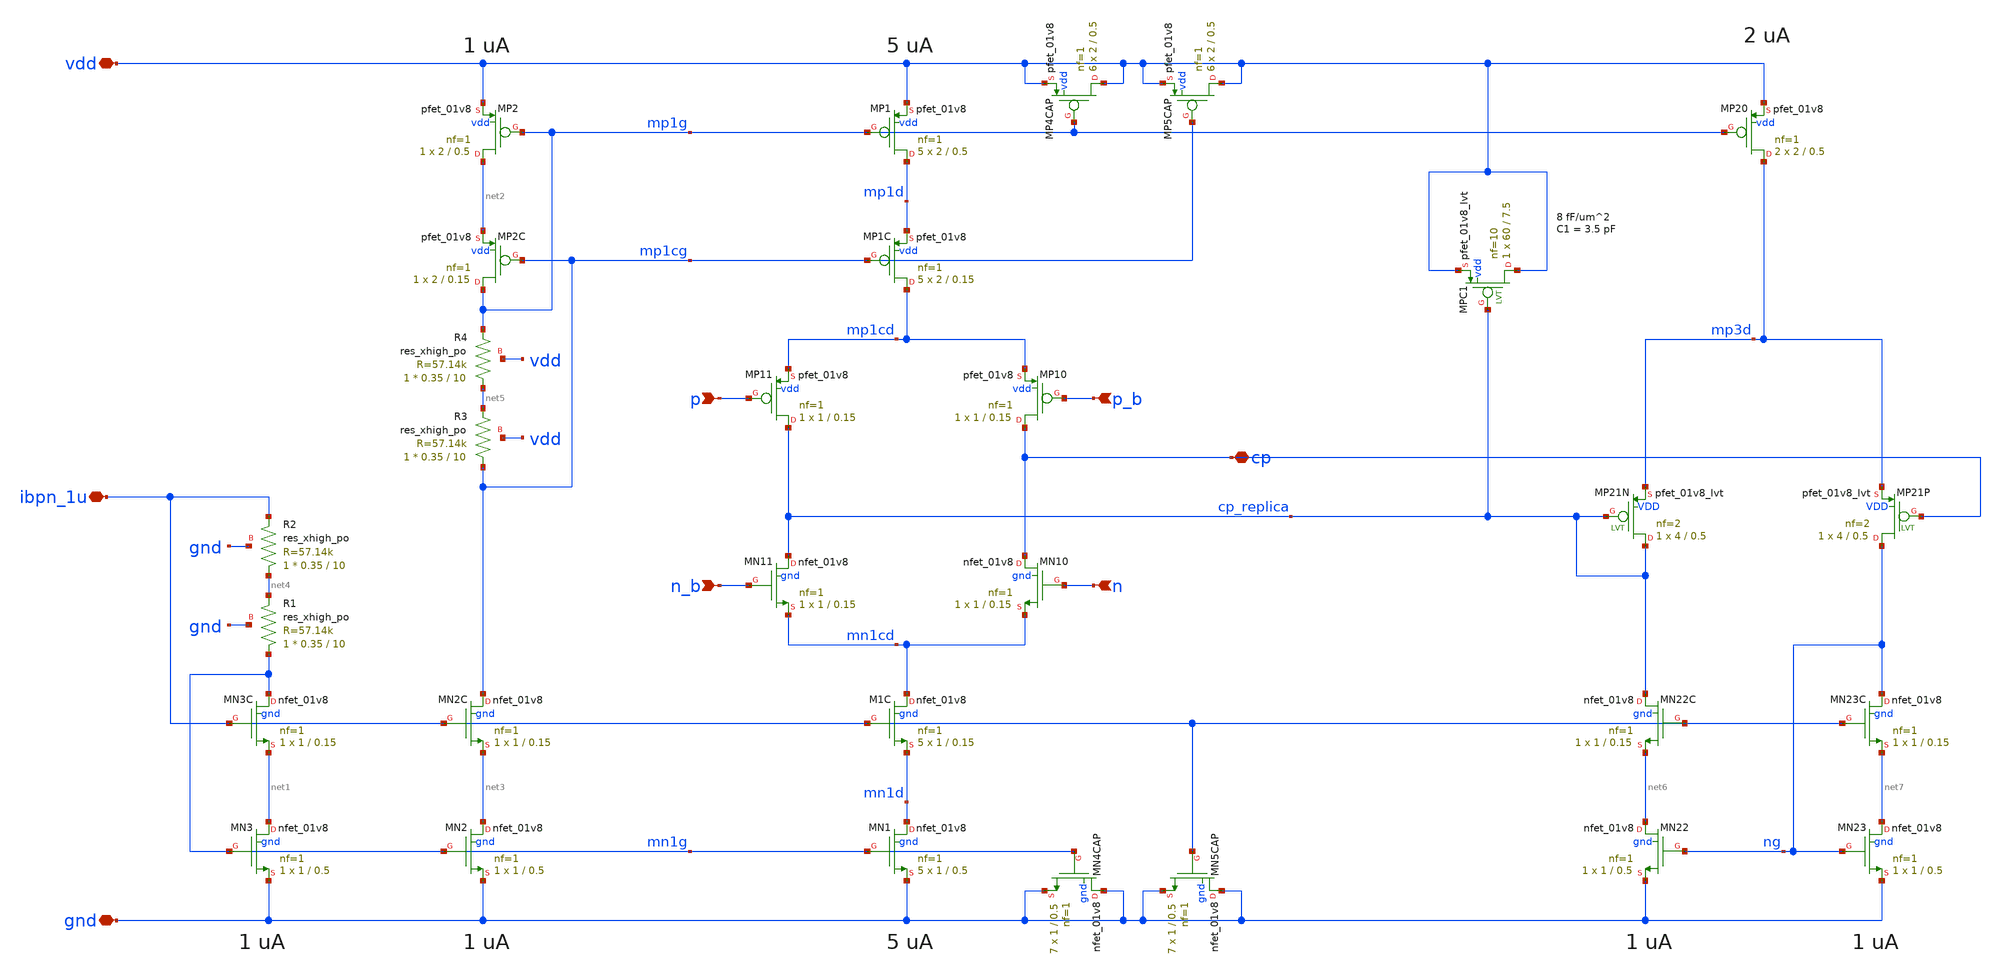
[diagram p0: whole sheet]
** sch_path: xschem/ejf_pll96_chp.sch
**.subckt ejf_pll96_chp vdd gnd ibpn_1u cp p n_b p_b n
*.iopin vdd
*.iopin gnd
*.iopin ibpn_1u
*.iopin cp
*.ipin p
*.ipin n_b
*.ipin p_b
*.ipin n
XMN3 net1 mn1g gnd gnd sky130_fd_pr__nfet_01v8 L=0.5 W=1 nf=1 ad='int((nf+1)/2) * W/nf * 0.29' as='int((nf+2)/2) * W/nf * 0.29'
+ pd='2*int((nf+1)/2) * (W/nf + 0.29)' ps='2*int((nf+2)/2) * (W/nf + 0.29)' nrd='0.29 / W' nrs='0.29 / W'
+ sa=0 sb=0 sd=0 mult=1 m=1
XMN3C mn1g ibpn_1u net1 gnd sky130_fd_pr__nfet_01v8 L=0.15 W=1 nf=1 ad='int((nf+1)/2) * W/nf * 0.29'
+ as='int((nf+2)/2) * W/nf * 0.29' pd='2*int((nf+1)/2) * (W/nf + 0.29)' ps='2*int((nf+2)/2) * (W/nf + 0.29)'
+ nrd='0.29 / W' nrs='0.29 / W' sa=0 sb=0 sd=0 mult=1 m=1
XMP2 net2 mp1g vdd vdd sky130_fd_pr__pfet_01v8 L=0.5 W=2 nf=1 ad='int((nf+1)/2) * W/nf * 0.29' as='int((nf+2)/2) * W/nf * 0.29'
+ pd='2*int((nf+1)/2) * (W/nf + 0.29)' ps='2*int((nf+2)/2) * (W/nf + 0.29)' nrd='0.29 / W' nrs='0.29 / W'
+ sa=0 sb=0 sd=0 mult=1 m=1
XMN2 net3 mn1g gnd gnd sky130_fd_pr__nfet_01v8 L=0.5 W=1 nf=1 ad='int((nf+1)/2) * W/nf * 0.29' as='int((nf+2)/2) * W/nf * 0.29'
+ pd='2*int((nf+1)/2) * (W/nf + 0.29)' ps='2*int((nf+2)/2) * (W/nf + 0.29)' nrd='0.29 / W' nrs='0.29 / W'
+ sa=0 sb=0 sd=0 mult=1 m=1
XMN2C mp1cg ibpn_1u net3 gnd sky130_fd_pr__nfet_01v8 L=0.15 W=1 nf=1 ad='int((nf+1)/2) * W/nf * 0.29'
+ as='int((nf+2)/2) * W/nf * 0.29' pd='2*int((nf+1)/2) * (W/nf + 0.29)' ps='2*int((nf+2)/2) * (W/nf + 0.29)'
+ nrd='0.29 / W' nrs='0.29 / W' sa=0 sb=0 sd=0 mult=1 m=1
XMP1 mp1d mp1g vdd vdd sky130_fd_pr__pfet_01v8 L=0.5 W=2 nf=1 ad='int((nf+1)/2) * W/nf * 0.29' as='int((nf+2)/2) * W/nf * 0.29'
+ pd='2*int((nf+1)/2) * (W/nf + 0.29)' ps='2*int((nf+2)/2) * (W/nf + 0.29)' nrd='0.29 / W' nrs='0.29 / W'
+ sa=0 sb=0 sd=0 mult=5 m=5
XMP2C mp1g mp1cg net2 vdd sky130_fd_pr__pfet_01v8 L=0.15 W=2 nf=1 ad='int((nf+1)/2) * W/nf * 0.29' as='int((nf+2)/2) * W/nf * 0.29'
+ pd='2*int((nf+1)/2) * (W/nf + 0.29)' ps='2*int((nf+2)/2) * (W/nf + 0.29)' nrd='0.29 / W' nrs='0.29 / W'
+ sa=0 sb=0 sd=0 mult=1 m=1
XMP1C mp1cd mp1cg mp1d vdd sky130_fd_pr__pfet_01v8 L=0.15 W=2 nf=1 ad='int((nf+1)/2) * W/nf * 0.29' as='int((nf+2)/2) * W/nf * 0.29'
+ pd='2*int((nf+1)/2) * (W/nf + 0.29)' ps='2*int((nf+2)/2) * (W/nf + 0.29)' nrd='0.29 / W' nrs='0.29 / W'
+ sa=0 sb=0 sd=0 mult=5 m=5
XMN1 mn1d mn1g gnd gnd sky130_fd_pr__nfet_01v8 L=0.5 W=1 nf=1 ad='int((nf+1)/2) * W/nf * 0.29' as='int((nf+2)/2) * W/nf * 0.29'
+ pd='2*int((nf+1)/2) * (W/nf + 0.29)' ps='2*int((nf+2)/2) * (W/nf + 0.29)' nrd='0.29 / W' nrs='0.29 / W'
+ sa=0 sb=0 sd=0 mult=5 m=5
XM1C mn1cd ibpn_1u mn1d gnd sky130_fd_pr__nfet_01v8 L=0.15 W=1 nf=1 ad='int((nf+1)/2) * W/nf * 0.29'
+ as='int((nf+2)/2) * W/nf * 0.29' pd='2*int((nf+1)/2) * (W/nf + 0.29)' ps='2*int((nf+2)/2) * (W/nf + 0.29)'
+ nrd='0.29 / W' nrs='0.29 / W' sa=0 sb=0 sd=0 mult=5 m=5
XR1 mn1g net4 gnd sky130_fd_pr__res_xhigh_po W=0.35 L=10 mult=1 m=1
XR2 net4 ibpn_1u gnd sky130_fd_pr__res_xhigh_po W=0.35 L=10 mult=1 m=1
XR3 mp1cg net5 vdd sky130_fd_pr__res_xhigh_po W=0.35 L=10 mult=1 m=1
XR4 net5 mp1g vdd sky130_fd_pr__res_xhigh_po W=0.35 L=10 mult=1 m=1
XMP11 cp_replica p mp1cd vdd sky130_fd_pr__pfet_01v8 L=0.15 W=1 nf=1 ad='int((nf+1)/2) * W/nf * 0.29'
+ as='int((nf+2)/2) * W/nf * 0.29' pd='2*int((nf+1)/2) * (W/nf + 0.29)' ps='2*int((nf+2)/2) * (W/nf + 0.29)'
+ nrd='0.29 / W' nrs='0.29 / W' sa=0 sb=0 sd=0 mult=1 m=1
XMN11 cp_replica n_b mn1cd gnd sky130_fd_pr__nfet_01v8 L=0.15 W=1 nf=1 ad='int((nf+1)/2) * W/nf * 0.29'
+ as='int((nf+2)/2) * W/nf * 0.29' pd='2*int((nf+1)/2) * (W/nf + 0.29)' ps='2*int((nf+2)/2) * (W/nf + 0.29)'
+ nrd='0.29 / W' nrs='0.29 / W' sa=0 sb=0 sd=0 mult=1 m=1
XMP10 cp p_b mp1cd vdd sky130_fd_pr__pfet_01v8 L=0.15 W=1 nf=1 ad='int((nf+1)/2) * W/nf * 0.29' as='int((nf+2)/2) * W/nf * 0.29'
+ pd='2*int((nf+1)/2) * (W/nf + 0.29)' ps='2*int((nf+2)/2) * (W/nf + 0.29)' nrd='0.29 / W' nrs='0.29 / W'
+ sa=0 sb=0 sd=0 mult=1 m=1
XMN10 cp n mn1cd gnd sky130_fd_pr__nfet_01v8 L=0.15 W=1 nf=1 ad='int((nf+1)/2) * W/nf * 0.29' as='int((nf+2)/2) * W/nf * 0.29'
+ pd='2*int((nf+1)/2) * (W/nf + 0.29)' ps='2*int((nf+2)/2) * (W/nf + 0.29)' nrd='0.29 / W' nrs='0.29 / W'
+ sa=0 sb=0 sd=0 mult=1 m=1
XMN4CAP gnd mn1g gnd gnd sky130_fd_pr__nfet_01v8 L=0.5 W=1 nf=1 ad='int((nf+1)/2) * W/nf * 0.29' as='int((nf+2)/2) * W/nf * 0.29'
+ pd='2*int((nf+1)/2) * (W/nf + 0.29)' ps='2*int((nf+2)/2) * (W/nf + 0.29)' nrd='0.29 / W' nrs='0.29 / W'
+ sa=0 sb=0 sd=0 mult=7 m=7
XMP4CAP vdd mp1g vdd vdd sky130_fd_pr__pfet_01v8 L=0.5 W=2 nf=1 ad='int((nf+1)/2) * W/nf * 0.29' as='int((nf+2)/2) * W/nf * 0.29'
+ pd='2*int((nf+1)/2) * (W/nf + 0.29)' ps='2*int((nf+2)/2) * (W/nf + 0.29)' nrd='0.29 / W' nrs='0.29 / W'
+ sa=0 sb=0 sd=0 mult=6 m=6
XMP5CAP vdd mp1cg vdd vdd sky130_fd_pr__pfet_01v8 L=0.5 W=2 nf=1 ad='int((nf+1)/2) * W/nf * 0.29' as='int((nf+2)/2) * W/nf * 0.29'
+ pd='2*int((nf+1)/2) * (W/nf + 0.29)' ps='2*int((nf+2)/2) * (W/nf + 0.29)' nrd='0.29 / W' nrs='0.29 / W'
+ sa=0 sb=0 sd=0 mult=6 m=6
XMN5CAP gnd ibpn_1u gnd gnd sky130_fd_pr__nfet_01v8 L=0.5 W=1 nf=1 ad='int((nf+1)/2) * W/nf * 0.29' as='int((nf+2)/2) * W/nf * 0.29'
+ pd='2*int((nf+1)/2) * (W/nf + 0.29)' ps='2*int((nf+2)/2) * (W/nf + 0.29)' nrd='0.29 / W' nrs='0.29 / W'
+ sa=0 sb=0 sd=0 mult=7 m=7
XMP20 mp3d mp1g vdd vdd sky130_fd_pr__pfet_01v8 L=0.5 W=2 nf=1 ad='int((nf+1)/2) * W/nf * 0.29' as='int((nf+2)/2) * W/nf * 0.29'
+ pd='2*int((nf+1)/2) * (W/nf + 0.29)' ps='2*int((nf+2)/2) * (W/nf + 0.29)' nrd='0.29 / W' nrs='0.29 / W'
+ sa=0 sb=0 sd=0 mult=2 m=2
XMN22C cp_replica ibpn_1u net6 gnd sky130_fd_pr__nfet_01v8 L=0.15 W=1 nf=1 ad='int((nf+1)/2) * W/nf * 0.29'
+ as='int((nf+2)/2) * W/nf * 0.29' pd='2*int((nf+1)/2) * (W/nf + 0.29)' ps='2*int((nf+2)/2) * (W/nf + 0.29)'
+ nrd='0.29 / W' nrs='0.29 / W' sa=0 sb=0 sd=0 mult=1 m=1
XMN23C ng ibpn_1u net7 gnd sky130_fd_pr__nfet_01v8 L=0.15 W=1 nf=1 ad='int((nf+1)/2) * W/nf * 0.29' as='int((nf+2)/2) * W/nf * 0.29'
+ pd='2*int((nf+1)/2) * (W/nf + 0.29)' ps='2*int((nf+2)/2) * (W/nf + 0.29)' nrd='0.29 / W' nrs='0.29 / W'
+ sa=0 sb=0 sd=0 mult=1 m=1
XMP21N cp_replica cp_replica mp3d VDD sky130_fd_pr__pfet_01v8_lvt L=0.5 W=4 nf=2 ad='int((nf+1)/2) * W/nf * 0.29'
+ as='int((nf+2)/2) * W/nf * 0.29' pd='2*int((nf+1)/2) * (W/nf + 0.29)' ps='2*int((nf+2)/2) * (W/nf + 0.29)'
+ nrd='0.29 / W' nrs='0.29 / W' sa=0 sb=0 sd=0 mult=1 m=1
XMP21P ng cp mp3d VDD sky130_fd_pr__pfet_01v8_lvt L=0.5 W=4 nf=2 ad='int((nf+1)/2) * W/nf * 0.29' as='int((nf+2)/2) * W/nf * 0.29'
+ pd='2*int((nf+1)/2) * (W/nf + 0.29)' ps='2*int((nf+2)/2) * (W/nf + 0.29)' nrd='0.29 / W' nrs='0.29 / W'
+ sa=0 sb=0 sd=0 mult=1 m=1
XMN23 net7 ng gnd gnd sky130_fd_pr__nfet_01v8 L=0.5 W=1 nf=1 ad='int((nf+1)/2) * W/nf * 0.29' as='int((nf+2)/2) * W/nf * 0.29'
+ pd='2*int((nf+1)/2) * (W/nf + 0.29)' ps='2*int((nf+2)/2) * (W/nf + 0.29)' nrd='0.29 / W' nrs='0.29 / W'
+ sa=0 sb=0 sd=0 mult=1 m=1
XMN22 net6 ng gnd gnd sky130_fd_pr__nfet_01v8 L=0.5 W=1 nf=1 ad='int((nf+1)/2) * W/nf * 0.29' as='int((nf+2)/2) * W/nf * 0.29'
+ pd='2*int((nf+1)/2) * (W/nf + 0.29)' ps='2*int((nf+2)/2) * (W/nf + 0.29)' nrd='0.29 / W' nrs='0.29 / W'
+ sa=0 sb=0 sd=0 mult=1 m=1
XMPC1 vdd cp_replica vdd vdd sky130_fd_pr__pfet_01v8_lvt L=7.5 W=60 nf=10 ad='int((nf+1)/2) * W/nf * 0.29'
+ as='int((nf+2)/2) * W/nf * 0.29' pd='2*int((nf+1)/2) * (W/nf + 0.29)' ps='2*int((nf+2)/2) * (W/nf + 0.29)'
+ nrd='0.29 / W' nrs='0.29 / W' sa=0 sb=0 sd=0 mult=1 m=1
**.ends
.end
